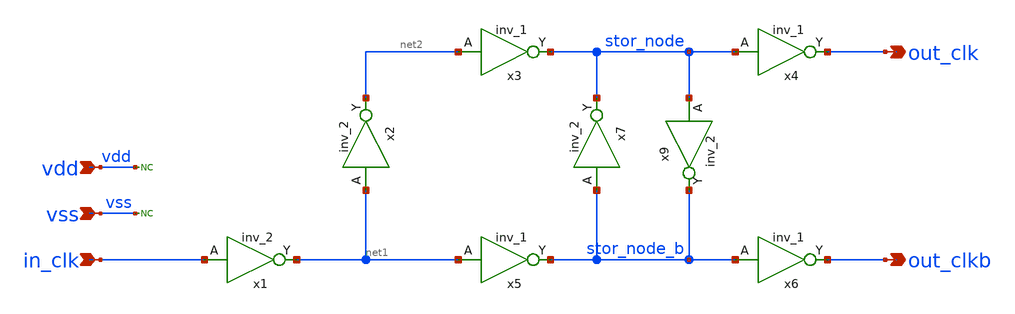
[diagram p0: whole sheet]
** sch_path: pll/pll_sync_clkb/xschem/pll_sync_clkb.sch
**.subckt pll_sync_clkb out_clk out_clkb vdd vss in_clk
*.opin out_clk
*.opin out_clkb
*.ipin vdd
*.ipin vss
*.ipin in_clk
x1 in_clk vss vss vdd vdd net1 sky130_fd_sc_hd__inv_2
x2 net1 vss vss vdd vdd net2 sky130_fd_sc_hd__inv_2
x4 stor_node vss vss vdd vdd out_clk sky130_fd_sc_hd__inv_1
x6 stor_node_b vss vss vdd vdd out_clkb sky130_fd_sc_hd__inv_1
x7 stor_node_b vss vss vdd vdd stor_node sky130_fd_sc_hd__inv_2
x9 stor_node vss vss vdd vdd stor_node_b sky130_fd_sc_hd__inv_2
x3 net2 vss vss vdd vdd stor_node sky130_fd_sc_hd__inv_1
x5 net1 vss vss vdd vdd stor_node_b sky130_fd_sc_hd__inv_1
* noconn vdd
* noconn vss
**** begin user architecture code

.options wnflag=1
.include $::SKYWATER_MODELS/cells/nfet_01v8/sky130_fd_pr__nfet_01v8__tt.corner.spice
.include $::SKYWATER_MODELS/cells/nfet_01v8_lvt/sky130_fd_pr__nfet_01v8_lvt__tt.corner.spice
.include $::SKYWATER_MODELS/cells/pfet_01v8/sky130_fd_pr__pfet_01v8__tt.corner.spice
.include $::SKYWATER_MODELS/cells/nfet_03v3_nvt/sky130_fd_pr__nfet_03v3_nvt__tt.corner.spice
.include $::SKYWATER_MODELS/cells/nfet_05v0_nvt/sky130_fd_pr__nfet_05v0_nvt__tt.corner.spice
.include $::SKYWATER_MODELS/cells/esd_nfet_01v8/sky130_fd_pr__esd_nfet_01v8__tt.corner.spice
.include $::SKYWATER_MODELS/cells/pfet_01v8_lvt/sky130_fd_pr__pfet_01v8_lvt__tt.corner.spice
.include $::SKYWATER_MODELS/cells/pfet_01v8_hvt/sky130_fd_pr__pfet_01v8_hvt__tt.corner.spice
.include $::SKYWATER_MODELS/cells/esd_pfet_g5v0d10v5/sky130_fd_pr__esd_pfet_g5v0d10v5__tt.corner.spice
.include $::SKYWATER_MODELS/cells/pfet_g5v0d10v5/sky130_fd_pr__pfet_g5v0d10v5__tt.corner.spice
.include $::SKYWATER_MODELS/cells/pfet_g5v0d16v0/sky130_fd_pr__pfet_g5v0d16v0__tt.corner.spice
.include $::SKYWATER_MODELS/cells/nfet_g5v0d10v5/sky130_fd_pr__nfet_g5v0d10v5__tt.corner.spice
.include $::SKYWATER_MODELS/cells/nfet_g5v0d16v0/sky130_fd_pr__nfet_g5v0d16v0__tt_discrete.corner.spice
.include $::SKYWATER_MODELS/cells/esd_nfet_g5v0d10v5/sky130_fd_pr__esd_nfet_g5v0d10v5__tt.corner.spice
.include $::SKYWATER_MODELS/models/corners/tt/nonfet.spice

.include $::SKYWATER_MODELS/cells/cap_var_hvt/sky130_fd_pr__cap_var_hvt.model.spice

* Mismatch parameters
.include $::SKYWATER_MODELS/cells/nfet_01v8/sky130_fd_pr__nfet_01v8__mismatch.corner.spice
.include $::SKYWATER_MODELS/cells/pfet_01v8/sky130_fd_pr__pfet_01v8__mismatch.corner.spice
.include $::SKYWATER_MODELS/cells/nfet_01v8_lvt/sky130_fd_pr__nfet_01v8_lvt__mismatch.corner.spice
.include $::SKYWATER_MODELS/cells/pfet_01v8_lvt/sky130_fd_pr__pfet_01v8_lvt__mismatch.corner.spice
.include $::SKYWATER_MODELS/cells/pfet_01v8_hvt/sky130_fd_pr__pfet_01v8_hvt__mismatch.corner.spice
.include $::SKYWATER_MODELS/cells/nfet_g5v0d10v5/sky130_fd_pr__nfet_g5v0d10v5__mismatch.corner.spice
.include $::SKYWATER_MODELS/cells/pfet_g5v0d10v5/sky130_fd_pr__pfet_g5v0d10v5__mismatch.corner.spice
.include $::SKYWATER_MODELS/cells/nfet_05v0_nvt/sky130_fd_pr__nfet_05v0_nvt__mismatch.corner.spice
.include $::SKYWATER_MODELS/cells/nfet_03v3_nvt/sky130_fd_pr__nfet_03v3_nvt__mismatch.corner.spice

* Resistor$::SKYWATER_MODELS/Capacitor
.include $::SKYWATER_MODELS/models/r+c/res_typical__cap_typical.spice
.include $::SKYWATER_MODELS/models/r+c/res_typical__cap_typical__lin.spice

* Special cells
.include $::SKYWATER_MODELS/models/corners/tt/specialized_cells.spice

* All models
.include $::SKYWATER_MODELS/models/all.spice

* Corner
.include $::SKYWATER_MODELS/models/corners/tt/rf.spice

* .include $::SKYWATER_STDCELLS/cells/
.include $::SKYWATER_STDCELLS/cells/and2/sky130_fd_sc_hd__and2_1.spice
.include $::SKYWATER_STDCELLS/cells/and2/sky130_fd_sc_hd__and2_2.spice
.include $::SKYWATER_STDCELLS_HS/cells/and2/sky130_fd_sc_hs__and2_1.spice
.include $::SKYWATER_STDCELLS_HS/cells/and2/sky130_fd_sc_hs__and2_2.spice

.include $::SKYWATER_STDCELLS/cells/nand2/sky130_fd_sc_hd__nand2_1.spice
.include $::SKYWATER_STDCELLS/cells/nand2/sky130_fd_sc_hd__nand2_2.spice
.include $::SKYWATER_STDCELLS_HS/cells/nand2/sky130_fd_sc_hs__nand2_1.spice
.include $::SKYWATER_STDCELLS_HS/cells/nand2/sky130_fd_sc_hs__nand2_2.spice

.include $::SKYWATER_STDCELLS/cells/or2/sky130_fd_sc_hd__or2_1.spice
.include $::SKYWATER_STDCELLS/cells/or2/sky130_fd_sc_hd__or2_2.spice
.include $::SKYWATER_STDCELLS_HS/cells/or2/sky130_fd_sc_hs__or2_1.spice
.include $::SKYWATER_STDCELLS_HS/cells/or2/sky130_fd_sc_hs__or2_2.spice

.include $::SKYWATER_STDCELLS/cells/buf/sky130_fd_sc_hd__buf_1.spice
.include $::SKYWATER_STDCELLS_HS/cells/buf/sky130_fd_sc_hs__buf_1.spice

.include $::SKYWATER_STDCELLS/cells/dfrbp/sky130_fd_sc_hd__dfrbp_1.spice
.include $::SKYWATER_STDCELLS/cells/dfrbp/sky130_fd_sc_hd__dfrbp_2.spice
.include $::SKYWATER_STDCELLS_HS/cells/dfrbp/sky130_fd_sc_hs__dfrbp_1.spice
.include $::SKYWATER_STDCELLS_HS/cells/dfrbp/sky130_fd_sc_hs__dfrbp_2.spice

.include $::SKYWATER_STDCELLS/cells/inv/sky130_fd_sc_hd__inv_1.spice
.include $::SKYWATER_STDCELLS/cells/inv/sky130_fd_sc_hd__inv_2.spice
.include $::SKYWATER_STDCELLS/cells/inv/sky130_fd_sc_hd__inv_4.spice
.include $::SKYWATER_STDCELLS/cells/inv/sky130_fd_sc_hd__inv_8.spice
.include $::SKYWATER_STDCELLS/cells/inv/sky130_fd_sc_hd__inv_16.spice
.include $::SKYWATER_STDCELLS_HS/cells/inv/sky130_fd_sc_hs__inv_1.spice
.include $::SKYWATER_STDCELLS_HS/cells/inv/sky130_fd_sc_hs__inv_2.spice
.include $::SKYWATER_STDCELLS_HS/cells/inv/sky130_fd_sc_hs__inv_4.spice
.include $::SKYWATER_STDCELLS_HS/cells/inv/sky130_fd_sc_hs__inv_8.spice
.include $::SKYWATER_STDCELLS_HS/cells/inv/sky130_fd_sc_hs__inv_16.spice

.include $::SKYWATER_STDCELLS/cells/mux2/sky130_fd_sc_hd__mux2_2.spice
.include $::SKYWATER_STDCELLS/cells/nand2/sky130_fd_sc_hd__nand2_1.spice

.include $::SKYWATER_STDCELLS/cells/tap/sky130_fd_sc_hd__tap_2.spice
.include $::SKYWATER_STDCELLS/cells/tapvpwrvgnd/sky130_fd_sc_hd__tapvpwrvgnd_1.spice

**** end user architecture code
**.ends
.end
